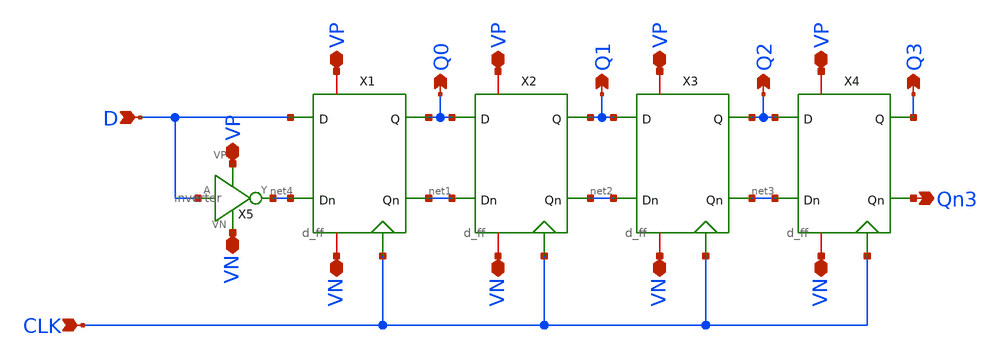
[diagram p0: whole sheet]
** sch_path: mp2/shift_reg.sch
**.subckt shift_reg VP VP VP VP VP VN VN VN VN VN D CLK Q0 Q1 Q2 Q3 Qn3
*.iopin VP
*.iopin VP
*.iopin VP
*.iopin VP
*.iopin VP
*.iopin VN
*.iopin VN
*.iopin VN
*.iopin VN
*.iopin VN
*.ipin D
*.ipin CLK
*.opin Q0
*.opin Q1
*.opin Q2
*.opin Q3
*.opin Qn3
X5 VP D net4 VN inverter
X1 VP Q0 D net4 net1 VN CLK d_ff
X2 VP Q1 Q0 net1 net2 VN CLK d_ff
X3 VP Q2 Q1 net2 net3 VN CLK d_ff
X4 VP Q3 Q2 net3 Qn3 VN CLK d_ff
**.ends

* expanding   symbol:  /home/dt/Documents/madvlsi/mp1/inverter.sym # of pins=4
** sym_path: final/schematics/inverter.sym
** sch_path: final/schematics/inverter.sch
.subckt inverter VP A Y VN
*.ipin A
*.iopin VP
*.iopin VN
*.opin Y
XM1 Y A VN VN sky130_fd_pr__nfet_01v8 L=0.15 W=1 nf=1 ad='int((nf+1)/2) * W/nf * 0.29' as='int((nf+2)/2) * W/nf * 0.29'
+ pd='2*int((nf+1)/2) * (W/nf + 0.29)' ps='2*int((nf+2)/2) * (W/nf + 0.29)' nrd='0.29 / W' nrs='0.29 / W'
+ sa=0 sb=0 sd=0 mult=1 m=1
XM2 Y A VP VP sky130_fd_pr__pfet_01v8 L=0.15 W=1 nf=1 ad='int((nf+1)/2) * W/nf * 0.29' as='int((nf+2)/2) * W/nf * 0.29'
+ pd='2*int((nf+1)/2) * (W/nf + 0.29)' ps='2*int((nf+2)/2) * (W/nf + 0.29)' nrd='0.29 / W' nrs='0.29 / W'
+ sa=0 sb=0 sd=0 mult=1 m=1
.ends


* expanding   symbol:  d_ff.sym # of pins=7
** sym_path: mp2/d_ff.sym
** sch_path: mp2/d_ff.sch
.subckt d_ff VP Q D Dn Qn VN CLK
*.ipin D
*.ipin Dn
*.ipin CLK
*.iopin VN
*.iopin VP
*.opin Qn
*.opin Q
XM1 net1 CLK Dn VDD sky130_fd_pr__pfet_01v8 L=0.45 W=1 nf=1 ad='int((nf+1)/2) * W/nf * 0.29' as='int((nf+2)/2) * W/nf * 0.29'
+ pd='2*int((nf+1)/2) * (W/nf + 0.29)' ps='2*int((nf+2)/2) * (W/nf + 0.29)' nrd='0.29 / W' nrs='0.29 / W'
+ sa=0 sb=0 sd=0 mult=1 m=1
XM2 VP net4 net1 VDD sky130_fd_pr__pfet_01v8 L=0.15 W=1 nf=1 ad='int((nf+1)/2) * W/nf * 0.29' as='int((nf+2)/2) * W/nf * 0.29'
+ pd='2*int((nf+1)/2) * (W/nf + 0.29)' ps='2*int((nf+2)/2) * (W/nf + 0.29)' nrd='0.29 / W' nrs='0.29 / W'
+ sa=0 sb=0 sd=0 mult=1 m=1
XM3 net2 CLK VP VDD sky130_fd_pr__pfet_01v8 L=0.15 W=1 nf=1 ad='int((nf+1)/2) * W/nf * 0.29' as='int((nf+2)/2) * W/nf * 0.29'
+ pd='2*int((nf+1)/2) * (W/nf + 0.29)' ps='2*int((nf+2)/2) * (W/nf + 0.29)' nrd='0.29 / W' nrs='0.29 / W'
+ sa=0 sb=0 sd=0 mult=1 m=1
XM4 Qn Q net2 VDD sky130_fd_pr__pfet_01v8 L=0.15 W=1 nf=1 ad='int((nf+1)/2) * W/nf * 0.29' as='int((nf+2)/2) * W/nf * 0.29'
+ pd='2*int((nf+1)/2) * (W/nf + 0.29)' ps='2*int((nf+2)/2) * (W/nf + 0.29)' nrd='0.29 / W' nrs='0.29 / W'
+ sa=0 sb=0 sd=0 mult=1 m=1
XM5 net4 CLK D VDD sky130_fd_pr__pfet_01v8 L=0.45 W=1 nf=1 ad='int((nf+1)/2) * W/nf * 0.29' as='int((nf+2)/2) * W/nf * 0.29'
+ pd='2*int((nf+1)/2) * (W/nf + 0.29)' ps='2*int((nf+2)/2) * (W/nf + 0.29)' nrd='0.29 / W' nrs='0.29 / W'
+ sa=0 sb=0 sd=0 mult=1 m=1
XM6 VP net1 net4 VDD sky130_fd_pr__pfet_01v8 L=0.15 W=1 nf=1 ad='int((nf+1)/2) * W/nf * 0.29' as='int((nf+2)/2) * W/nf * 0.29'
+ pd='2*int((nf+1)/2) * (W/nf + 0.29)' ps='2*int((nf+2)/2) * (W/nf + 0.29)' nrd='0.29 / W' nrs='0.29 / W'
+ sa=0 sb=0 sd=0 mult=1 m=1
XM7 net3 CLK VP VDD sky130_fd_pr__pfet_01v8 L=0.15 W=1 nf=1 ad='int((nf+1)/2) * W/nf * 0.29' as='int((nf+2)/2) * W/nf * 0.29'
+ pd='2*int((nf+1)/2) * (W/nf + 0.29)' ps='2*int((nf+2)/2) * (W/nf + 0.29)' nrd='0.29 / W' nrs='0.29 / W'
+ sa=0 sb=0 sd=0 mult=1 m=1
XM8 Q Qn net3 VDD sky130_fd_pr__pfet_01v8 L=0.15 W=1 nf=1 ad='int((nf+1)/2) * W/nf * 0.29' as='int((nf+2)/2) * W/nf * 0.29'
+ pd='2*int((nf+1)/2) * (W/nf + 0.29)' ps='2*int((nf+2)/2) * (W/nf + 0.29)' nrd='0.29 / W' nrs='0.29 / W'
+ sa=0 sb=0 sd=0 mult=1 m=1
XM9 VN CLK net5 GND sky130_fd_pr__nfet_01v8 L=0.15 W=1 nf=1 ad='int((nf+1)/2) * W/nf * 0.29' as='int((nf+2)/2) * W/nf * 0.29'
+ pd='2*int((nf+1)/2) * (W/nf + 0.29)' ps='2*int((nf+2)/2) * (W/nf + 0.29)' nrd='0.29 / W' nrs='0.29 / W'
+ sa=0 sb=0 sd=0 mult=1 m=1
XM10 net4 net1 net5 GND sky130_fd_pr__nfet_01v8 L=0.15 W=1 nf=1 ad='int((nf+1)/2) * W/nf * 0.29' as='int((nf+2)/2) * W/nf * 0.29'
+ pd='2*int((nf+1)/2) * (W/nf + 0.29)' ps='2*int((nf+2)/2) * (W/nf + 0.29)' nrd='0.29 / W' nrs='0.29 / W'
+ sa=0 sb=0 sd=0 mult=1 m=1
XM11 net4 CLK Q GND sky130_fd_pr__nfet_01v8 L=0.45 W=1 nf=1 ad='int((nf+1)/2) * W/nf * 0.29' as='int((nf+2)/2) * W/nf * 0.29'
+ pd='2*int((nf+1)/2) * (W/nf + 0.29)' ps='2*int((nf+2)/2) * (W/nf + 0.29)' nrd='0.29 / W' nrs='0.29 / W'
+ sa=0 sb=0 sd=0 mult=1 m=1
XM12 VN Qn Q GND sky130_fd_pr__nfet_01v8 L=0.15 W=1 nf=1 ad='int((nf+1)/2) * W/nf * 0.29' as='int((nf+2)/2) * W/nf * 0.29'
+ pd='2*int((nf+1)/2) * (W/nf + 0.29)' ps='2*int((nf+2)/2) * (W/nf + 0.29)' nrd='0.29 / W' nrs='0.29 / W'
+ sa=0 sb=0 sd=0 mult=1 m=1
XM13 VN CLK net6 GND sky130_fd_pr__nfet_01v8 L=0.15 W=1 nf=1 ad='int((nf+1)/2) * W/nf * 0.29' as='int((nf+2)/2) * W/nf * 0.29'
+ pd='2*int((nf+1)/2) * (W/nf + 0.29)' ps='2*int((nf+2)/2) * (W/nf + 0.29)' nrd='0.29 / W' nrs='0.29 / W'
+ sa=0 sb=0 sd=0 mult=1 m=1
XM14 net1 net4 net6 GND sky130_fd_pr__nfet_01v8 L=0.15 W=1 nf=1 ad='int((nf+1)/2) * W/nf * 0.29' as='int((nf+2)/2) * W/nf * 0.29'
+ pd='2*int((nf+1)/2) * (W/nf + 0.29)' ps='2*int((nf+2)/2) * (W/nf + 0.29)' nrd='0.29 / W' nrs='0.29 / W'
+ sa=0 sb=0 sd=0 mult=1 m=1
XM15 net1 CLK Qn GND sky130_fd_pr__nfet_01v8 L=0.45 W=1 nf=1 ad='int((nf+1)/2) * W/nf * 0.29' as='int((nf+2)/2) * W/nf * 0.29'
+ pd='2*int((nf+1)/2) * (W/nf + 0.29)' ps='2*int((nf+2)/2) * (W/nf + 0.29)' nrd='0.29 / W' nrs='0.29 / W'
+ sa=0 sb=0 sd=0 mult=1 m=1
XM16 VN Q Qn GND sky130_fd_pr__nfet_01v8 L=0.15 W=1 nf=1 ad='int((nf+1)/2) * W/nf * 0.29' as='int((nf+2)/2) * W/nf * 0.29'
+ pd='2*int((nf+1)/2) * (W/nf + 0.29)' ps='2*int((nf+2)/2) * (W/nf + 0.29)' nrd='0.29 / W' nrs='0.29 / W'
+ sa=0 sb=0 sd=0 mult=1 m=1
.ends

.end
